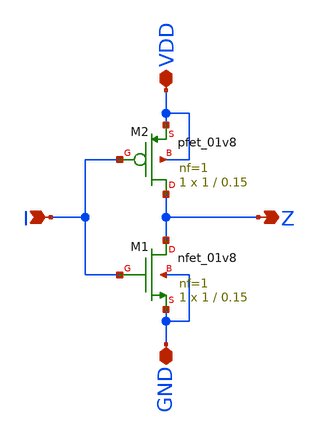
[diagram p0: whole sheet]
** sch_path: sky130_cells/Practice/Example_Inverter/Example_Inverter.sch
**.subckt Example_Inverter I Z VDD GND
*.ipin I
*.opin Z
*.iopin VDD
*.iopin GND
XM1 Z I GND GND sky130_fd_pr__nfet_01v8 L=0.15 W=1 nf=1 ad='int((nf+1)/2) * W/nf * 0.29' as='int((nf+2)/2) * W/nf * 0.29'
+ pd='2*int((nf+1)/2) * (W/nf + 0.29)' ps='2*int((nf+2)/2) * (W/nf + 0.29)' nrd='0.29 / W' nrs='0.29 / W'
+ sa=0 sb=0 sd=0 mult=1 m=1
XM2 Z I VDD VDD sky130_fd_pr__pfet_01v8 L=0.15 W=1 nf=1 ad='int((nf+1)/2) * W/nf * 0.29' as='int((nf+2)/2) * W/nf * 0.29'
+ pd='2*int((nf+1)/2) * (W/nf + 0.29)' ps='2*int((nf+2)/2) * (W/nf + 0.29)' nrd='0.29 / W' nrs='0.29 / W'
+ sa=0 sb=0 sd=0 mult=1 m=1
**.ends
.end
